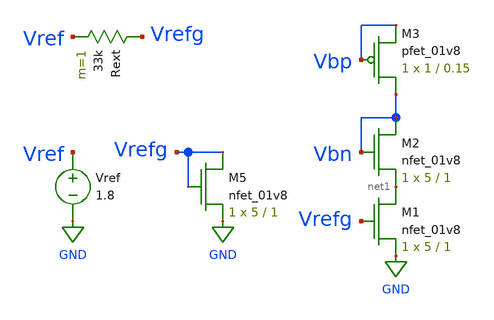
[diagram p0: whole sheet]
** sch_path: self_bias_gen.sch
**.subckt self_bias_gen
XM1 net1 Vrefg GND GND sky130_fd_pr__nfet_01v8 L=1 W=5 nf=1 ad='int((nf+1)/2) * W/nf * 0.29' as='int((nf+2)/2) * W/nf * 0.29'
+ pd='2*int((nf+1)/2) * (W/nf + 0.29)' ps='2*int((nf+2)/2) * (W/nf + 0.29)' nrd='0.29 / W' nrs='0.29 / W'
+ sa=0 sb=0 sd=0 mult=1 m=1
Rext Vrefg Vref 33k m=1
Vref Vref GND 1.8
XM2 Vbn Vbn net1 GND sky130_fd_pr__nfet_01v8 L=1 W=5 nf=1 ad='int((nf+1)/2) * W/nf * 0.29' as='int((nf+2)/2) * W/nf * 0.29'
+ pd='2*int((nf+1)/2) * (W/nf + 0.29)' ps='2*int((nf+2)/2) * (W/nf + 0.29)' nrd='0.29 / W' nrs='0.29 / W'
+ sa=0 sb=0 sd=0 mult=1 m=1
XM5 Vrefg Vrefg GND GND sky130_fd_pr__nfet_01v8 L=1 W=5 nf=1 ad='int((nf+1)/2) * W/nf * 0.29' as='int((nf+2)/2) * W/nf * 0.29'
+ pd='2*int((nf+1)/2) * (W/nf + 0.29)' ps='2*int((nf+2)/2) * (W/nf + 0.29)' nrd='0.29 / W' nrs='0.29 / W'
+ sa=0 sb=0 sd=0 mult=1 m=1
XM3 Vbn Vbp Vbp VDD sky130_fd_pr__pfet_01v8 L=0.15 W=1 nf=1 ad='int((nf+1)/2) * W/nf * 0.29' as='int((nf+2)/2) * W/nf * 0.29'
+ pd='2*int((nf+1)/2) * (W/nf + 0.29)' ps='2*int((nf+2)/2) * (W/nf + 0.29)' nrd='0.29 / W' nrs='0.29 / W'
+ sa=0 sb=0 sd=0 mult=1 m=1
**.ends
.GLOBAL GND
.end
